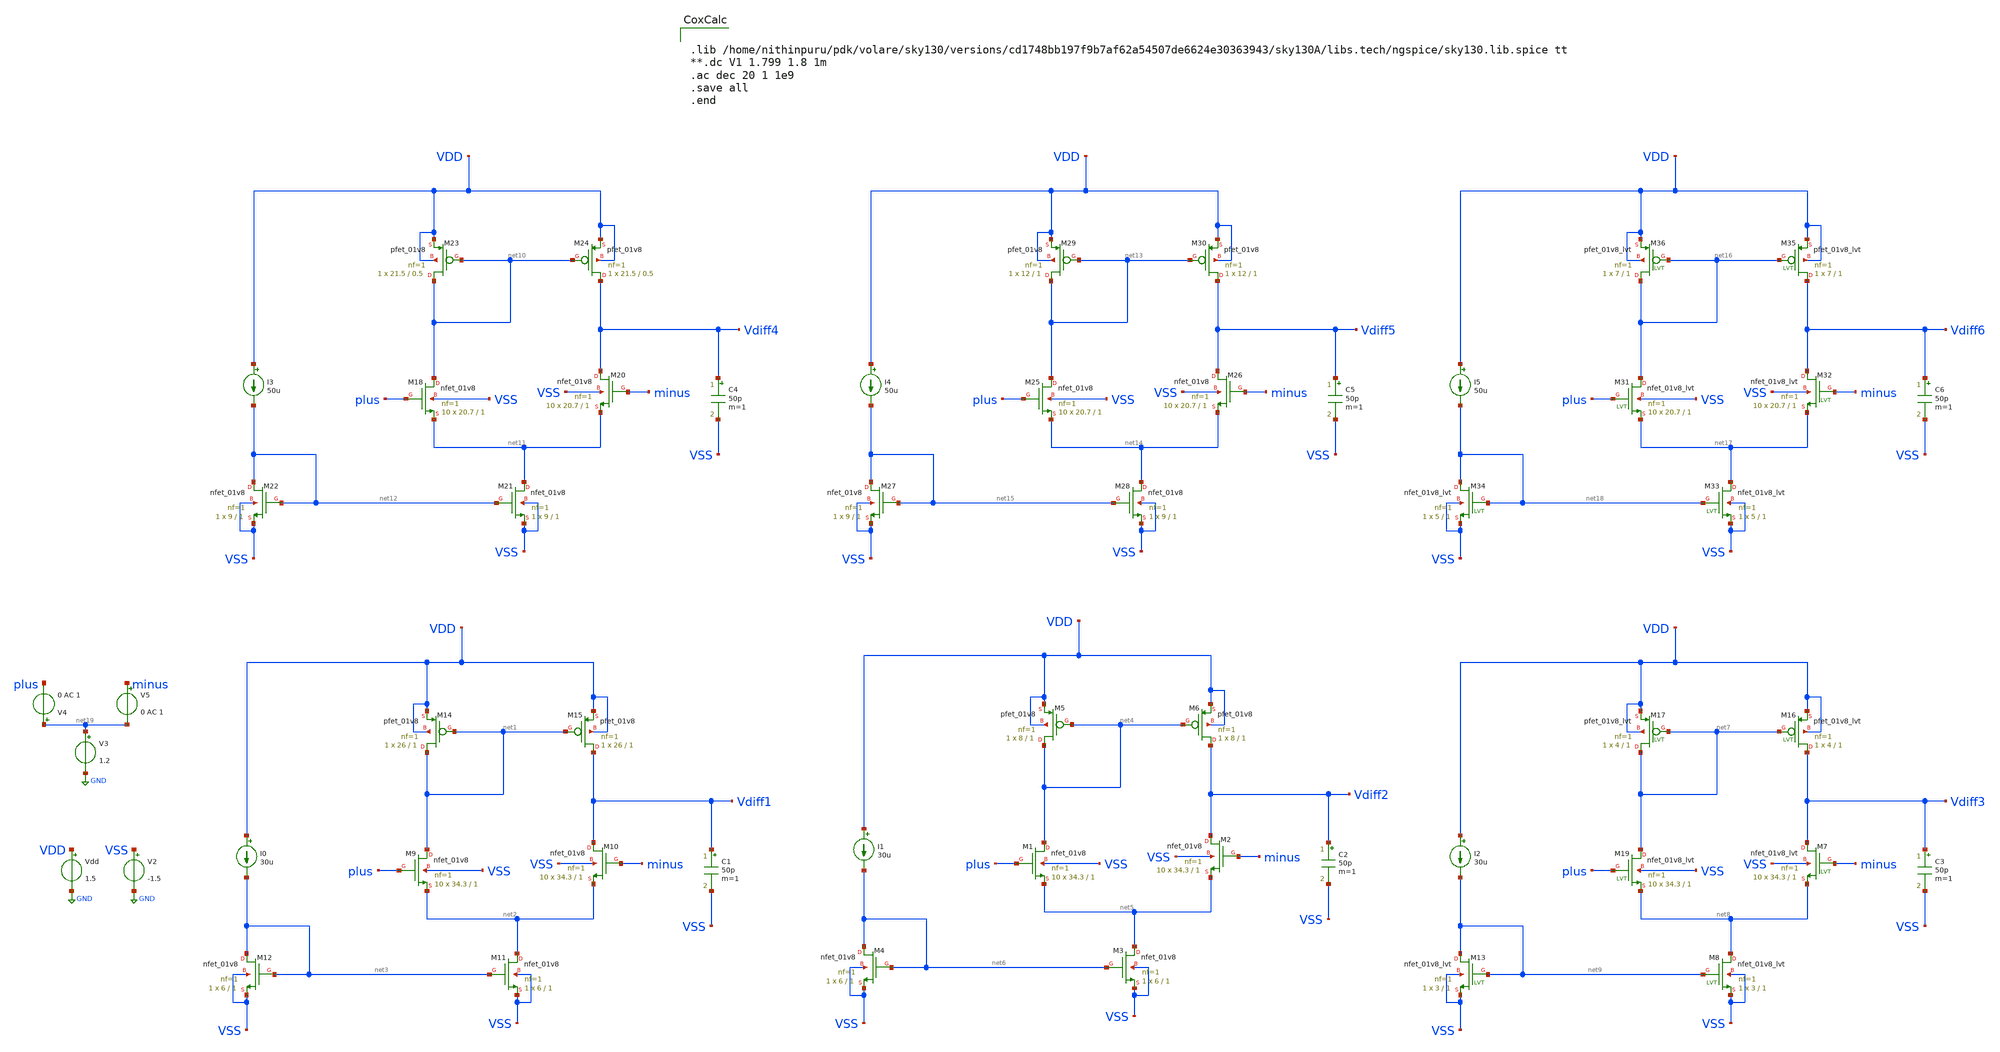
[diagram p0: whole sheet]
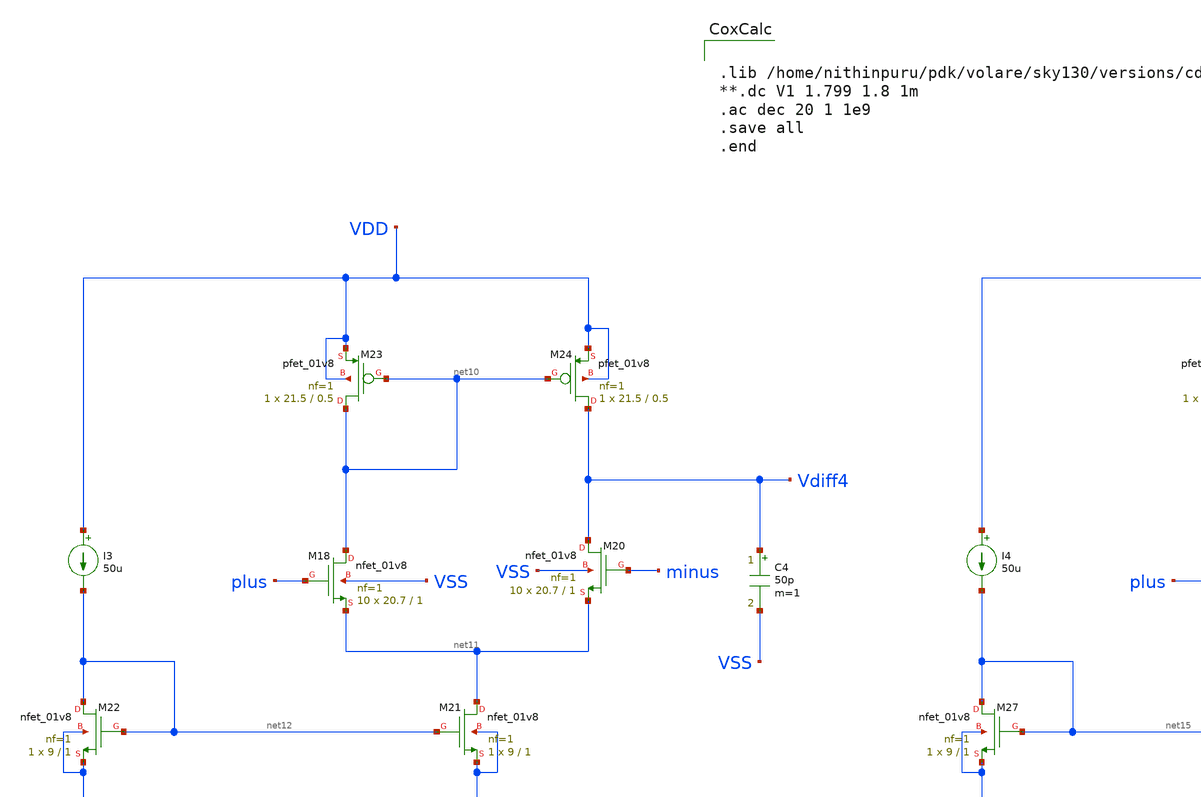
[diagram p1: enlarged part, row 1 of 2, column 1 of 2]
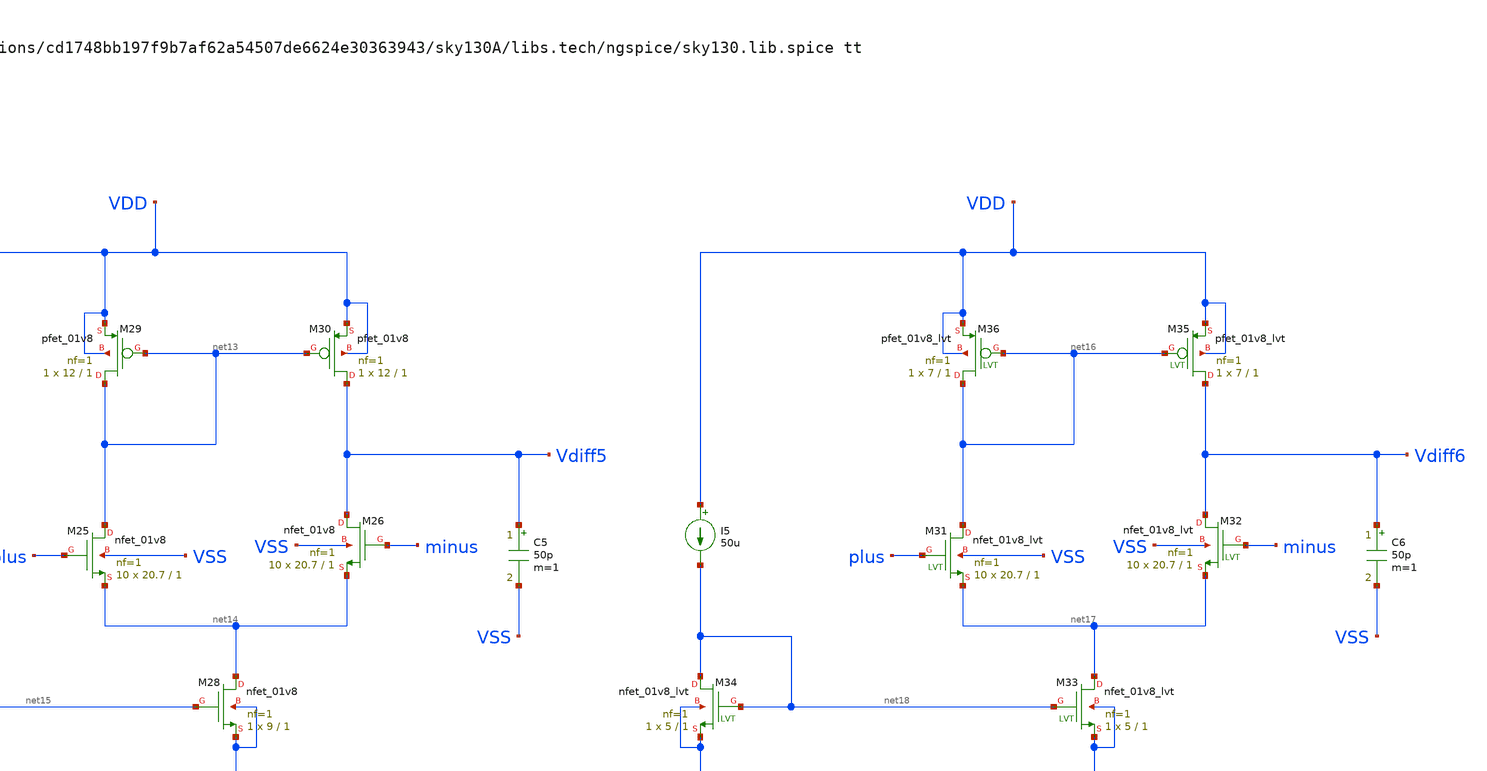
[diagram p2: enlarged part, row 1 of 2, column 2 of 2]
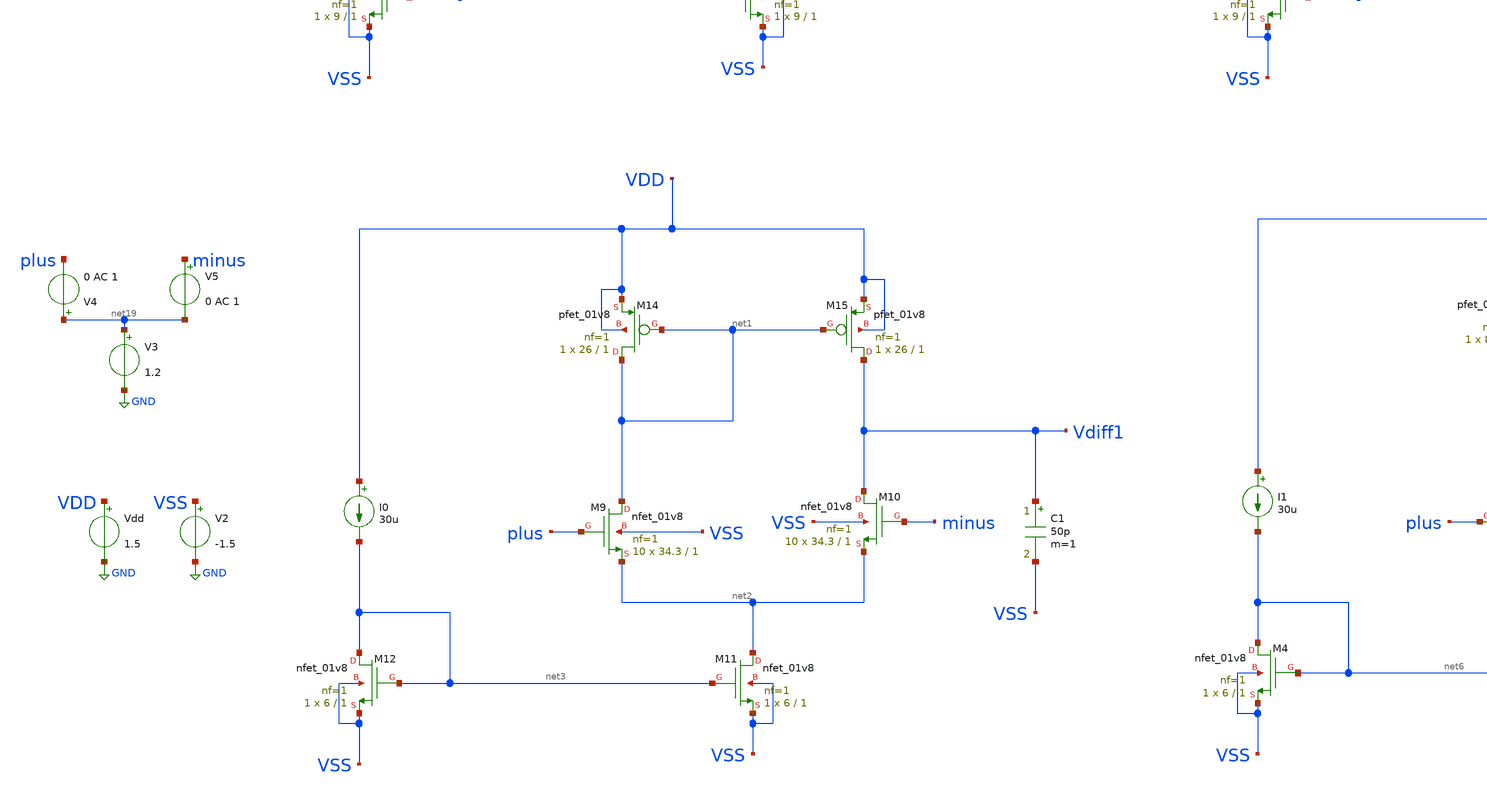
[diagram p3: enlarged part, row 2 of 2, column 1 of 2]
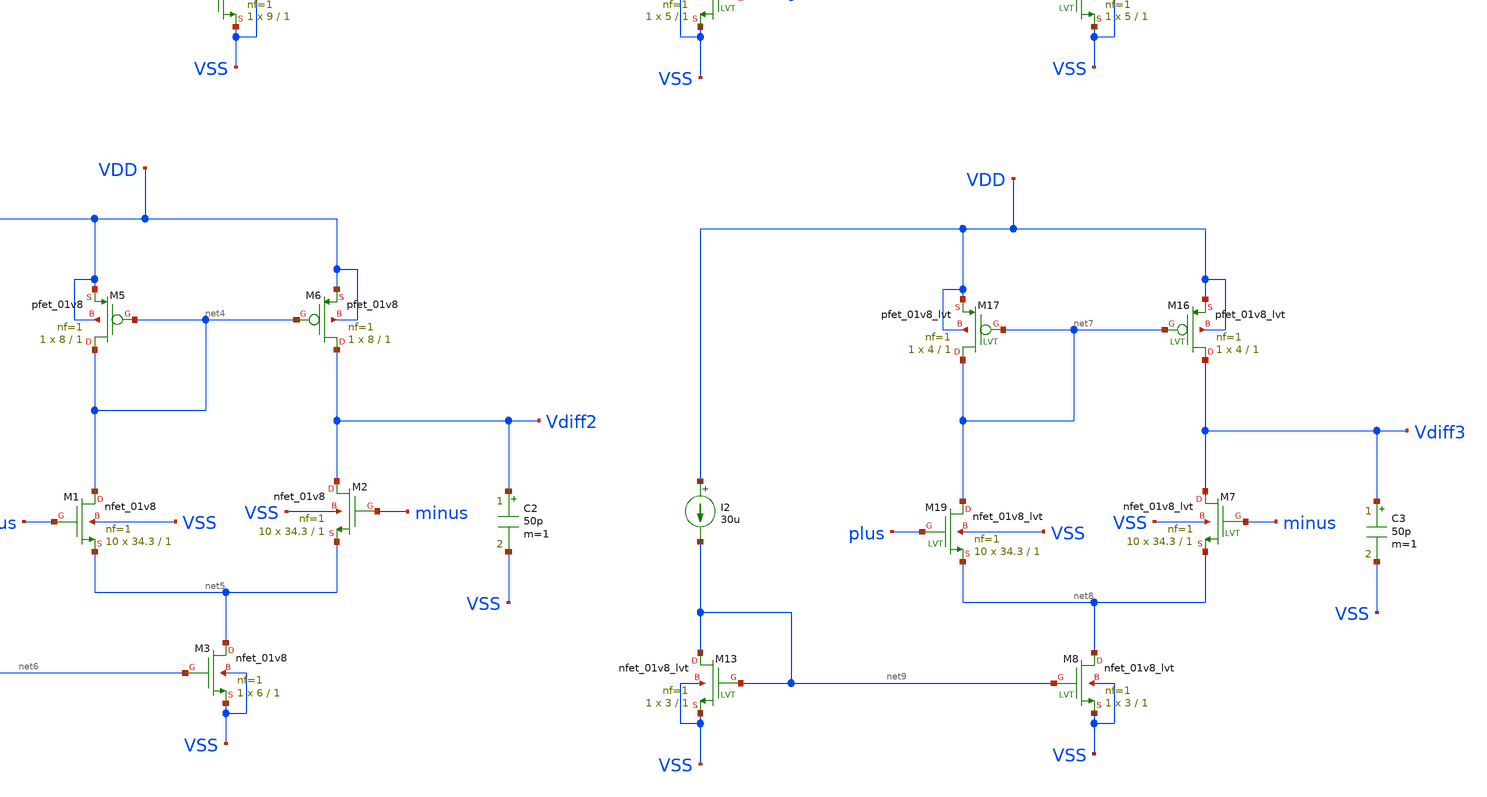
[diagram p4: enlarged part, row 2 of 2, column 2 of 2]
** sch_path: Schematics/Differential_amp.sch
**.subckt Differential_amp
XM9 net1 plus net2 VSS sky130_fd_pr__nfet_01v8 L=1 W=34.3 nf=1 ad='int((nf+1)/2) * W/nf * 0.29' as='int((nf+2)/2) * W/nf * 0.29'
+ pd='2*int((nf+1)/2) * (W/nf + 0.29)' ps='2*int((nf+2)/2) * (W/nf + 0.29)' nrd='0.29 / W' nrs='0.29 / W'
+ sa=0 sb=0 sd=0 mult=10 m=10
XM10 Vdiff1 minus net2 VSS sky130_fd_pr__nfet_01v8 L=1 W=34.3 nf=1 ad='int((nf+1)/2) * W/nf * 0.29' as='int((nf+2)/2) * W/nf * 0.29'
+ pd='2*int((nf+1)/2) * (W/nf + 0.29)' ps='2*int((nf+2)/2) * (W/nf + 0.29)' nrd='0.29 / W' nrs='0.29 / W'
+ sa=0 sb=0 sd=0 mult=10 m=10
XM12 net3 net3 VSS VSS sky130_fd_pr__nfet_01v8 L=1 W=6 nf=1 ad='int((nf+1)/2) * W/nf * 0.29' as='int((nf+2)/2) * W/nf * 0.29'
+ pd='2*int((nf+1)/2) * (W/nf + 0.29)' ps='2*int((nf+2)/2) * (W/nf + 0.29)' nrd='0.29 / W' nrs='0.29 / W'
+ sa=0 sb=0 sd=0 mult=1 m=1
XM14 net1 net1 VDD VDD sky130_fd_pr__pfet_01v8 L=1 W=26 nf=1 ad='int((nf+1)/2) * W/nf * 0.29' as='int((nf+2)/2) * W/nf * 0.29'
+ pd='2*int((nf+1)/2) * (W/nf + 0.29)' ps='2*int((nf+2)/2) * (W/nf + 0.29)' nrd='0.29 / W' nrs='0.29 / W'
+ sa=0 sb=0 sd=0 mult=1 m=1
C1 Vdiff1 VSS 50p m=1
I0 VDD net3 30u
XM5 net4 net4 VDD VDD sky130_fd_pr__pfet_01v8 L=1 W=8 nf=1 ad='int((nf+1)/2) * W/nf * 0.29' as='int((nf+2)/2) * W/nf * 0.29'
+ pd='2*int((nf+1)/2) * (W/nf + 0.29)' ps='2*int((nf+2)/2) * (W/nf + 0.29)' nrd='0.29 / W' nrs='0.29 / W'
+ sa=0 sb=0 sd=0 mult=1 m=1
I1 VDD net6 30u
I2 VDD net9 30u
XM19 net7 plus net8 VSS sky130_fd_pr__nfet_01v8_lvt L=1 W=34.3 nf=1 ad='int((nf+1)/2) * W/nf * 0.29'
+ as='int((nf+2)/2) * W/nf * 0.29' pd='2*int((nf+1)/2) * (W/nf + 0.29)' ps='2*int((nf+2)/2) * (W/nf + 0.29)'
+ nrd='0.29 / W' nrs='0.29 / W' sa=0 sb=0 sd=0 mult=10 m=10
XM13 net9 net9 VSS VSS sky130_fd_pr__nfet_01v8_lvt L=1 W=3 nf=1 ad='int((nf+1)/2) * W/nf * 0.29' as='int((nf+2)/2) * W/nf * 0.29'
+ pd='2*int((nf+1)/2) * (W/nf + 0.29)' ps='2*int((nf+2)/2) * (W/nf + 0.29)' nrd='0.29 / W' nrs='0.29 / W'
+ sa=0 sb=0 sd=0 mult=1 m=1
XM17 net7 net7 VDD VDD sky130_fd_pr__pfet_01v8_lvt L=1 W=4 nf=1 ad='int((nf+1)/2) * W/nf * 0.29' as='int((nf+2)/2) * W/nf * 0.29'
+ pd='2*int((nf+1)/2) * (W/nf + 0.29)' ps='2*int((nf+2)/2) * (W/nf + 0.29)' nrd='0.29 / W' nrs='0.29 / W'
+ sa=0 sb=0 sd=0 mult=1 m=1
XM18 net10 plus net11 VSS sky130_fd_pr__nfet_01v8 L=1 W=20.7 nf=1 ad='int((nf+1)/2) * W/nf * 0.29' as='int((nf+2)/2) * W/nf * 0.29'
+ pd='2*int((nf+1)/2) * (W/nf + 0.29)' ps='2*int((nf+2)/2) * (W/nf + 0.29)' nrd='0.29 / W' nrs='0.29 / W'
+ sa=0 sb=0 sd=0 mult=10 m=10
XM21 net11 net12 VSS VSS sky130_fd_pr__nfet_01v8 L=1 W=9 nf=1 ad='int((nf+1)/2) * W/nf * 0.29' as='int((nf+2)/2) * W/nf * 0.29'
+ pd='2*int((nf+1)/2) * (W/nf + 0.29)' ps='2*int((nf+2)/2) * (W/nf + 0.29)' nrd='0.29 / W' nrs='0.29 / W'
+ sa=0 sb=0 sd=0 mult=1 m=1
XM22 net12 net12 VSS VSS sky130_fd_pr__nfet_01v8 L=1 W=9 nf=1 ad='int((nf+1)/2) * W/nf * 0.29' as='int((nf+2)/2) * W/nf * 0.29'
+ pd='2*int((nf+1)/2) * (W/nf + 0.29)' ps='2*int((nf+2)/2) * (W/nf + 0.29)' nrd='0.29 / W' nrs='0.29 / W'
+ sa=0 sb=0 sd=0 mult=1 m=1
XM23 net10 net10 VDD VDD sky130_fd_pr__pfet_01v8 L=0.5 W=21.5 nf=1 ad='int((nf+1)/2) * W/nf * 0.29' as='int((nf+2)/2) * W/nf * 0.29'
+ pd='2*int((nf+1)/2) * (W/nf + 0.29)' ps='2*int((nf+2)/2) * (W/nf + 0.29)' nrd='0.29 / W' nrs='0.29 / W'
+ sa=0 sb=0 sd=0 mult=1 m=1
C4 Vdiff4 VSS 50p m=1
I3 VDD net12 50u
XM29 net13 net13 VDD VDD sky130_fd_pr__pfet_01v8 L=1 W=12 nf=1 ad='int((nf+1)/2) * W/nf * 0.29' as='int((nf+2)/2) * W/nf * 0.29'
+ pd='2*int((nf+1)/2) * (W/nf + 0.29)' ps='2*int((nf+2)/2) * (W/nf + 0.29)' nrd='0.29 / W' nrs='0.29 / W'
+ sa=0 sb=0 sd=0 mult=1 m=1
C5 Vdiff5 VSS 50p m=1
I4 VDD net15 50u
C6 Vdiff6 VSS 50p m=1
I5 VDD net18 50u
XM31 net16 plus net17 VSS sky130_fd_pr__nfet_01v8_lvt L=1 W=20.7 nf=1 ad='int((nf+1)/2) * W/nf * 0.29'
+ as='int((nf+2)/2) * W/nf * 0.29' pd='2*int((nf+1)/2) * (W/nf + 0.29)' ps='2*int((nf+2)/2) * (W/nf + 0.29)'
+ nrd='0.29 / W' nrs='0.29 / W' sa=0 sb=0 sd=0 mult=10 m=10
XM34 net18 net18 VSS VSS sky130_fd_pr__nfet_01v8_lvt L=1 W=5 nf=1 ad='int((nf+1)/2) * W/nf * 0.29' as='int((nf+2)/2) * W/nf * 0.29'
+ pd='2*int((nf+1)/2) * (W/nf + 0.29)' ps='2*int((nf+2)/2) * (W/nf + 0.29)' nrd='0.29 / W' nrs='0.29 / W'
+ sa=0 sb=0 sd=0 mult=1 m=1
XM36 net16 net16 VDD VDD sky130_fd_pr__pfet_01v8_lvt L=1 W=7 nf=1 ad='int((nf+1)/2) * W/nf * 0.29' as='int((nf+2)/2) * W/nf * 0.29'
+ pd='2*int((nf+1)/2) * (W/nf + 0.29)' ps='2*int((nf+2)/2) * (W/nf + 0.29)' nrd='0.29 / W' nrs='0.29 / W'
+ sa=0 sb=0 sd=0 mult=1 m=1
XM20 Vdiff4 minus net11 VSS sky130_fd_pr__nfet_01v8 L=1 W=20.7 nf=1 ad='int((nf+1)/2) * W/nf * 0.29'
+ as='int((nf+2)/2) * W/nf * 0.29' pd='2*int((nf+1)/2) * (W/nf + 0.29)' ps='2*int((nf+2)/2) * (W/nf + 0.29)'
+ nrd='0.29 / W' nrs='0.29 / W' sa=0 sb=0 sd=0 mult=10 m=10
XM25 net13 plus net14 VSS sky130_fd_pr__nfet_01v8 L=1 W=20.7 nf=1 ad='int((nf+1)/2) * W/nf * 0.29' as='int((nf+2)/2) * W/nf * 0.29'
+ pd='2*int((nf+1)/2) * (W/nf + 0.29)' ps='2*int((nf+2)/2) * (W/nf + 0.29)' nrd='0.29 / W' nrs='0.29 / W'
+ sa=0 sb=0 sd=0 mult=10 m=10
XM26 Vdiff5 minus net14 VSS sky130_fd_pr__nfet_01v8 L=1 W=20.7 nf=1 ad='int((nf+1)/2) * W/nf * 0.29'
+ as='int((nf+2)/2) * W/nf * 0.29' pd='2*int((nf+1)/2) * (W/nf + 0.29)' ps='2*int((nf+2)/2) * (W/nf + 0.29)'
+ nrd='0.29 / W' nrs='0.29 / W' sa=0 sb=0 sd=0 mult=10 m=10
XM24 Vdiff4 net10 VDD VDD sky130_fd_pr__pfet_01v8 L=0.5 W=21.5 nf=1 ad='int((nf+1)/2) * W/nf * 0.29'
+ as='int((nf+2)/2) * W/nf * 0.29' pd='2*int((nf+1)/2) * (W/nf + 0.29)' ps='2*int((nf+2)/2) * (W/nf + 0.29)'
+ nrd='0.29 / W' nrs='0.29 / W' sa=0 sb=0 sd=0 mult=1 m=1
XM30 Vdiff5 net13 VDD VDD sky130_fd_pr__pfet_01v8 L=1 W=12 nf=1 ad='int((nf+1)/2) * W/nf * 0.29' as='int((nf+2)/2) * W/nf * 0.29'
+ pd='2*int((nf+1)/2) * (W/nf + 0.29)' ps='2*int((nf+2)/2) * (W/nf + 0.29)' nrd='0.29 / W' nrs='0.29 / W'
+ sa=0 sb=0 sd=0 mult=1 m=1
XM27 net15 net15 VSS VSS sky130_fd_pr__nfet_01v8 L=1 W=9 nf=1 ad='int((nf+1)/2) * W/nf * 0.29' as='int((nf+2)/2) * W/nf * 0.29'
+ pd='2*int((nf+1)/2) * (W/nf + 0.29)' ps='2*int((nf+2)/2) * (W/nf + 0.29)' nrd='0.29 / W' nrs='0.29 / W'
+ sa=0 sb=0 sd=0 mult=1 m=1
XM28 net14 net15 VSS VSS sky130_fd_pr__nfet_01v8 L=1 W=9 nf=1 ad='int((nf+1)/2) * W/nf * 0.29' as='int((nf+2)/2) * W/nf * 0.29'
+ pd='2*int((nf+1)/2) * (W/nf + 0.29)' ps='2*int((nf+2)/2) * (W/nf + 0.29)' nrd='0.29 / W' nrs='0.29 / W'
+ sa=0 sb=0 sd=0 mult=1 m=1
XM32 Vdiff6 minus net17 VSS sky130_fd_pr__nfet_01v8_lvt L=1 W=20.7 nf=1 ad='int((nf+1)/2) * W/nf * 0.29'
+ as='int((nf+2)/2) * W/nf * 0.29' pd='2*int((nf+1)/2) * (W/nf + 0.29)' ps='2*int((nf+2)/2) * (W/nf + 0.29)'
+ nrd='0.29 / W' nrs='0.29 / W' sa=0 sb=0 sd=0 mult=10 m=10
XM35 Vdiff6 net16 VDD VDD sky130_fd_pr__pfet_01v8_lvt L=1 W=7 nf=1 ad='int((nf+1)/2) * W/nf * 0.29' as='int((nf+2)/2) * W/nf * 0.29'
+ pd='2*int((nf+1)/2) * (W/nf + 0.29)' ps='2*int((nf+2)/2) * (W/nf + 0.29)' nrd='0.29 / W' nrs='0.29 / W'
+ sa=0 sb=0 sd=0 mult=1 m=1
XM33 net17 net18 VSS VSS sky130_fd_pr__nfet_01v8_lvt L=1 W=5 nf=1 ad='int((nf+1)/2) * W/nf * 0.29' as='int((nf+2)/2) * W/nf * 0.29'
+ pd='2*int((nf+1)/2) * (W/nf + 0.29)' ps='2*int((nf+2)/2) * (W/nf + 0.29)' nrd='0.29 / W' nrs='0.29 / W'
+ sa=0 sb=0 sd=0 mult=1 m=1
C2 Vdiff2 VSS 50p m=1
C3 Vdiff3 VSS 50p m=1
XM1 net4 plus net5 VSS sky130_fd_pr__nfet_01v8 L=1 W=34.3 nf=1 ad='int((nf+1)/2) * W/nf * 0.29' as='int((nf+2)/2) * W/nf * 0.29'
+ pd='2*int((nf+1)/2) * (W/nf + 0.29)' ps='2*int((nf+2)/2) * (W/nf + 0.29)' nrd='0.29 / W' nrs='0.29 / W'
+ sa=0 sb=0 sd=0 mult=10 m=10
XM2 Vdiff2 minus net5 VSS sky130_fd_pr__nfet_01v8 L=1 W=34.3 nf=1 ad='int((nf+1)/2) * W/nf * 0.29' as='int((nf+2)/2) * W/nf * 0.29'
+ pd='2*int((nf+1)/2) * (W/nf + 0.29)' ps='2*int((nf+2)/2) * (W/nf + 0.29)' nrd='0.29 / W' nrs='0.29 / W'
+ sa=0 sb=0 sd=0 mult=10 m=10
XM15 Vdiff1 net1 VDD VDD sky130_fd_pr__pfet_01v8 L=1 W=26 nf=1 ad='int((nf+1)/2) * W/nf * 0.29' as='int((nf+2)/2) * W/nf * 0.29'
+ pd='2*int((nf+1)/2) * (W/nf + 0.29)' ps='2*int((nf+2)/2) * (W/nf + 0.29)' nrd='0.29 / W' nrs='0.29 / W'
+ sa=0 sb=0 sd=0 mult=1 m=1
XM6 Vdiff2 net4 VDD VDD sky130_fd_pr__pfet_01v8 L=1 W=8 nf=1 ad='int((nf+1)/2) * W/nf * 0.29' as='int((nf+2)/2) * W/nf * 0.29'
+ pd='2*int((nf+1)/2) * (W/nf + 0.29)' ps='2*int((nf+2)/2) * (W/nf + 0.29)' nrd='0.29 / W' nrs='0.29 / W'
+ sa=0 sb=0 sd=0 mult=1 m=1
XM11 net2 net3 VSS VSS sky130_fd_pr__nfet_01v8 L=1 W=6 nf=1 ad='int((nf+1)/2) * W/nf * 0.29' as='int((nf+2)/2) * W/nf * 0.29'
+ pd='2*int((nf+1)/2) * (W/nf + 0.29)' ps='2*int((nf+2)/2) * (W/nf + 0.29)' nrd='0.29 / W' nrs='0.29 / W'
+ sa=0 sb=0 sd=0 mult=1 m=1
XM3 net5 net6 VSS VSS sky130_fd_pr__nfet_01v8 L=1 W=6 nf=1 ad='int((nf+1)/2) * W/nf * 0.29' as='int((nf+2)/2) * W/nf * 0.29'
+ pd='2*int((nf+1)/2) * (W/nf + 0.29)' ps='2*int((nf+2)/2) * (W/nf + 0.29)' nrd='0.29 / W' nrs='0.29 / W'
+ sa=0 sb=0 sd=0 mult=1 m=1
XM4 net6 net6 VSS VSS sky130_fd_pr__nfet_01v8 L=1 W=6 nf=1 ad='int((nf+1)/2) * W/nf * 0.29' as='int((nf+2)/2) * W/nf * 0.29'
+ pd='2*int((nf+1)/2) * (W/nf + 0.29)' ps='2*int((nf+2)/2) * (W/nf + 0.29)' nrd='0.29 / W' nrs='0.29 / W'
+ sa=0 sb=0 sd=0 mult=1 m=1
XM7 Vdiff3 minus net8 VSS sky130_fd_pr__nfet_01v8_lvt L=1 W=34.3 nf=1 ad='int((nf+1)/2) * W/nf * 0.29'
+ as='int((nf+2)/2) * W/nf * 0.29' pd='2*int((nf+1)/2) * (W/nf + 0.29)' ps='2*int((nf+2)/2) * (W/nf + 0.29)'
+ nrd='0.29 / W' nrs='0.29 / W' sa=0 sb=0 sd=0 mult=10 m=10
XM16 Vdiff3 net7 VDD VDD sky130_fd_pr__pfet_01v8_lvt L=1 W=4 nf=1 ad='int((nf+1)/2) * W/nf * 0.29' as='int((nf+2)/2) * W/nf * 0.29'
+ pd='2*int((nf+1)/2) * (W/nf + 0.29)' ps='2*int((nf+2)/2) * (W/nf + 0.29)' nrd='0.29 / W' nrs='0.29 / W'
+ sa=0 sb=0 sd=0 mult=1 m=1
XM8 net8 net9 VSS VSS sky130_fd_pr__nfet_01v8_lvt L=1 W=3 nf=1 ad='int((nf+1)/2) * W/nf * 0.29' as='int((nf+2)/2) * W/nf * 0.29'
+ pd='2*int((nf+1)/2) * (W/nf + 0.29)' ps='2*int((nf+2)/2) * (W/nf + 0.29)' nrd='0.29 / W' nrs='0.29 / W'
+ sa=0 sb=0 sd=0 mult=1 m=1
V3 net19 GND 1.2
V4 net19 plus 0 AC 1
V5 minus net19 0 AC 1
Vdd VDD GND 1.5
V2 VSS GND -1.5
**** begin user architecture code


.lib /home/nithinpuru/pdk/volare/sky130/versions/cd1748bb197f9b7af62a54507de6624e30363943/sky130A/libs.tech/ngspice/sky130.lib.spice tt
**.dc V1 1.799 1.8 1m
.ac dec 20 1 1e9
.save all
.end

**** end user architecture code
**.ends
.GLOBAL GND
.end
